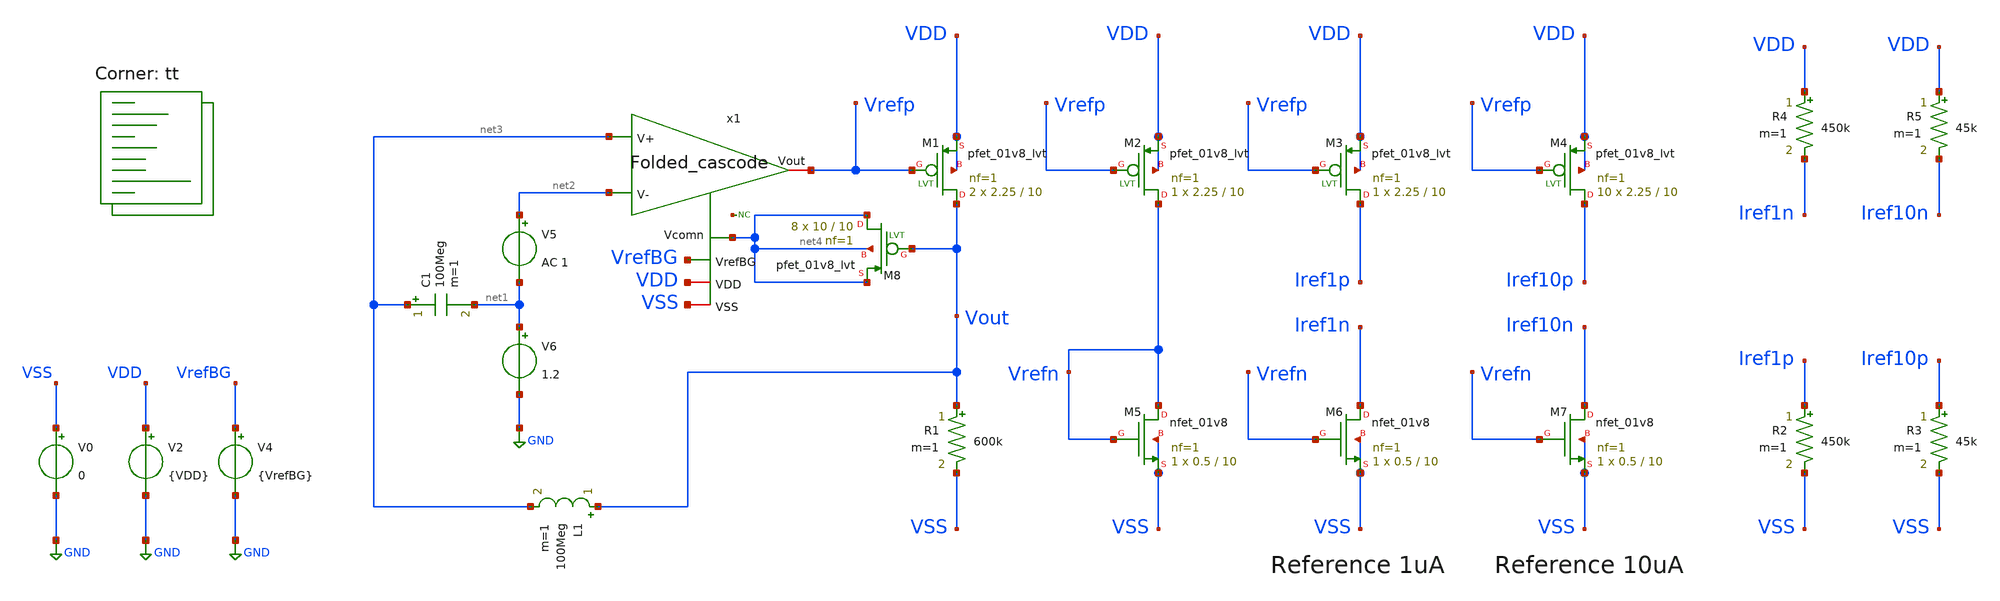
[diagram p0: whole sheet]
** sch_path: openfasoc/generators/curref-gen/sch/Current_reference_generator_AC.sch
**.subckt Current_reference_generator_AC
XM1 Vout Vrefp VDD VDD sky130_fd_pr__pfet_01v8_lvt L=10 W=2.25 nf=1 ad='int((1 + 1)/2) * 2.25 / 1 * 0.29'
+ as='int((1 + 2)/2) * 2.25 / 1 * 0.29' pd='2*int((1 + 1)/2) * (2.25 / 1 + 0.29)' ps='2*int((1 + 2)/2) * (2.25 / 1 + 0.29)'
+ nrd='0.29 / 2.25 ' nrs='0.29 / 2.25 ' sa=0 sb=0 sd=0 mult=2 m=2
R1 Vout VSS 600k m=1
XM2 Vrefn Vrefp VDD VDD sky130_fd_pr__pfet_01v8_lvt L=10 W=2.25 nf=1 ad='int((1 + 1)/2) * 2.25 / 1 * 0.29'
+ as='int((1 + 2)/2) * 2.25 / 1 * 0.29' pd='2*int((1 + 1)/2) * (2.25 / 1 + 0.29)' ps='2*int((1 + 2)/2) * (2.25 / 1 + 0.29)'
+ nrd='0.29 / 2.25 ' nrs='0.29 / 2.25 ' sa=0 sb=0 sd=0 mult=1 m=1
XM5 Vrefn Vrefn VSS VSS sky130_fd_pr__nfet_01v8 L=10 W=0.5 nf=1 ad='int((nf+1)/2) * W/nf * 0.29' as='int((nf+2)/2) * W/nf * 0.29'
+ pd='2*int((nf+1)/2) * (W/nf + 0.29)' ps='2*int((nf+2)/2) * (W/nf + 0.29)' nrd='0.29 / W' nrs='0.29 / W'
+ sa=0 sb=0 sd=0 mult=1 m=1
XM6 Iref1n Vrefn VSS VSS sky130_fd_pr__nfet_01v8 L=10 W=0.5 nf=1 ad='int((nf+1)/2) * W/nf * 0.29' as='int((nf+2)/2) * W/nf * 0.29'
+ pd='2*int((nf+1)/2) * (W/nf + 0.29)' ps='2*int((nf+2)/2) * (W/nf + 0.29)' nrd='0.29 / W' nrs='0.29 / W'
+ sa=0 sb=0 sd=0 mult=1 m=1
XM3 Iref1p Vrefp VDD VDD sky130_fd_pr__pfet_01v8_lvt L=10 W=2.25 nf=1 ad='int((1 + 1)/2) * 2.25 / 1 * 0.29'
+ as='int((1 + 2)/2) * 2.25 / 1 * 0.29' pd='2*int((1 + 1)/2) * (2.25 / 1 + 0.29)' ps='2*int((1 + 2)/2) * (2.25 / 1 + 0.29)'
+ nrd='0.29 / 2.25 ' nrs='0.29 / 2.25 ' sa=0 sb=0 sd=0 mult=1 m=1
XM7 Iref10n Vrefn VSS VSS sky130_fd_pr__nfet_01v8 L=10 W=0.5 nf=1 ad='int((nf+1)/2) * W/nf * 0.29' as='int((nf+2)/2) * W/nf * 0.29'
+ pd='2*int((nf+1)/2) * (W/nf + 0.29)' ps='2*int((nf+2)/2) * (W/nf + 0.29)' nrd='0.29 / W' nrs='0.29 / W'
+ sa=0 sb=0 sd=0 mult=1 m=1
XM4 Iref10p Vrefp VDD VDD sky130_fd_pr__pfet_01v8_lvt L=10 W=2.25 nf=1 ad='int((1 + 1)/2) * 2.25 / 1 * 0.29'
+ as='int((1 + 2)/2) * 2.25 / 1 * 0.29' pd='2*int((1 + 1)/2) * (2.25 / 1 + 0.29)' ps='2*int((1 + 2)/2) * (2.25 / 1 + 0.29)'
+ nrd='0.29 / 2.25 ' nrs='0.29 / 2.25 ' sa=0 sb=0 sd=0 mult=10 m=10
V0 VSS GND 0
V2 VDD GND {VDD}
V4 VrefBG GND {VrefBG}
R2 Iref1p VSS 450k m=1
R3 Iref10p VSS 45k m=1
R4 VDD Iref1n 450k m=1
R5 VDD Iref10n 45k m=1
L1 Vout net3 100Meg m=1
C1 net3 net1 100Meg m=1
V5 net2 net1 AC 1
V6 net1 GND 1.2
x1 Vrefp net3 net2 VrefBG VDD VSS net4 Folded_cascode
* noconn #net5
XM8 net4 Vout net4 net4 sky130_fd_pr__pfet_01v8_lvt L=10 W=10 nf=1 ad='int((1 + 1)/2) * 10 / 1 * 0.29'
+ as='int((1 + 2)/2) * 10 / 1 * 0.29' pd='2*int((1 + 1)/2) * (10 / 1 + 0.29)' ps='2*int((1 + 2)/2) * (10 / 1 + 0.29)'
+ nrd='0.29 / 10 ' nrs='0.29 / 10 ' sa=0 sb=0 sd=0 mult=8 m=8
**** begin user architecture code
.lib $::SKYWATER_MODELS/sky130.lib.spice tt



.param VDD=1.8
.param VrefBG=1.2

.save

.control

    op
    show

    write Current_reference_generator_AC.raw
    set appendwrite

    * run ac simulation
    ac dec 20 1 100e6

    * measure parameters
    let vout_mag = db(abs(v(Vout)))
    let phase = phase(v(Vout)) * 180/pi + 180

    meas ac A0 find vout_mag at=1k
    meas ac UGB when vout_mag=0 fall=1
    meas ac PM find phase when vout_mag=1

    plot (phase(v(Vout))*180/pi) db(Vout)

    write Current_reference_generator_AC.raw
.endc



**** end user architecture code
**.ends

* expanding   symbol:  /foss/designs/Folded_cascode/Folded_cascode.sym # of pins=7
** sym_path: openfasoc/generators/curref-gen/sch/Folded_cascode.sym
** sch_path: openfasoc/generators/curref-gen/sch/Folded_cascode.sch
.subckt Folded_cascode Vout V+ V- VrefBG VDD VSS Vcomn
*.ipin V+
*.ipin V-
*.ipin VrefBG
*.iopin VDD
*.iopin VSS
*.iopin Vout
*.iopin Vcomn
XM6 net2 V- net5 net5 sky130_fd_pr__nfet_01v8 L=1 W=1 nf=1 ad='int((nf+1)/2) * W/nf * 0.29' as='int((nf+2)/2) * W/nf * 0.29'
+ pd='2*int((nf+1)/2) * (W/nf + 0.29)' ps='2*int((nf+2)/2) * (W/nf + 0.29)' nrd='0.29 / W' nrs='0.29 / W'
+ sa=0 sb=0 sd=0 mult=20 m=20
XM7 Vout VB2 Vcomn VSS sky130_fd_pr__nfet_01v8 L=3 W=1 nf=1 ad='int((nf+1)/2) * W/nf * 0.29' as='int((nf+2)/2) * W/nf * 0.29'
+ pd='2*int((nf+1)/2) * (W/nf + 0.29)' ps='2*int((nf+2)/2) * (W/nf + 0.29)' nrd='0.29 / W' nrs='0.29 / W'
+ sa=0 sb=0 sd=0 mult=5 m=5
XM8 net4 VB2 net3 VSS sky130_fd_pr__nfet_01v8 L=3 W=1 nf=1 ad='int((nf+1)/2) * W/nf * 0.29' as='int((nf+2)/2) * W/nf * 0.29'
+ pd='2*int((nf+1)/2) * (W/nf + 0.29)' ps='2*int((nf+2)/2) * (W/nf + 0.29)' nrd='0.29 / W' nrs='0.29 / W'
+ sa=0 sb=0 sd=0 mult=5 m=5
XM9 Vcomn VP VSS VSS sky130_fd_pr__nfet_01v8 L=6.5 W=0.5 nf=1 ad='int((nf+1)/2) * W/nf * 0.29' as='int((nf+2)/2) * W/nf * 0.29'
+ pd='2*int((nf+1)/2) * (W/nf + 0.29)' ps='2*int((nf+2)/2) * (W/nf + 0.29)' nrd='0.29 / W' nrs='0.29 / W'
+ sa=0 sb=0 sd=0 mult=5 m=5
XM10 net3 VP VSS VSS sky130_fd_pr__nfet_01v8 L=6.5 W=0.5 nf=1 ad='int((nf+1)/2) * W/nf * 0.29' as='int((nf+2)/2) * W/nf * 0.29'
+ pd='2*int((nf+1)/2) * (W/nf + 0.29)' ps='2*int((nf+2)/2) * (W/nf + 0.29)' nrd='0.29 / W' nrs='0.29 / W'
+ sa=0 sb=0 sd=0 mult=5 m=5
XM11 net5 VP VSS VSS sky130_fd_pr__nfet_01v8 L=6.5 W=0.5 nf=1 ad='int((nf+1)/2) * W/nf * 0.29' as='int((nf+2)/2) * W/nf * 0.29'
+ pd='2*int((nf+1)/2) * (W/nf + 0.29)' ps='2*int((nf+2)/2) * (W/nf + 0.29)' nrd='0.29 / W' nrs='0.29 / W'
+ sa=0 sb=0 sd=0 mult=10 m=10
XM1 net1 V+ net5 net5 sky130_fd_pr__nfet_01v8 L=1 W=1 nf=1 ad='int((nf+1)/2) * W/nf * 0.29' as='int((nf+2)/2) * W/nf * 0.29'
+ pd='2*int((nf+1)/2) * (W/nf + 0.29)' ps='2*int((nf+2)/2) * (W/nf + 0.29)' nrd='0.29 / W' nrs='0.29 / W'
+ sa=0 sb=0 sd=0 mult=20 m=20
XM12 VP VP VSS VSS sky130_fd_pr__nfet_01v8 L=6.5 W=0.5 nf=1 ad='int((nf+1)/2) * W/nf * 0.29' as='int((nf+2)/2) * W/nf * 0.29'
+ pd='2*int((nf+1)/2) * (W/nf + 0.29)' ps='2*int((nf+2)/2) * (W/nf + 0.29)' nrd='0.29 / W' nrs='0.29 / W'
+ sa=0 sb=0 sd=0 mult=1 m=1
XM13 net6 VP VSS VSS sky130_fd_pr__nfet_01v8 L=6.5 W=0.5 nf=1 ad='int((nf+1)/2) * W/nf * 0.29' as='int((nf+2)/2) * W/nf * 0.29'
+ pd='2*int((nf+1)/2) * (W/nf + 0.29)' ps='2*int((nf+2)/2) * (W/nf + 0.29)' nrd='0.29 / W' nrs='0.29 / W'
+ sa=0 sb=0 sd=0 mult=1 m=1
XM17 VB2 VB2 VSS VSS sky130_fd_pr__nfet_01v8 L=18 W=0.42 nf=1 ad='int((nf+1)/2) * W/nf * 0.29' as='int((nf+2)/2) * W/nf * 0.29'
+ pd='2*int((nf+1)/2) * (W/nf + 0.29)' ps='2*int((nf+2)/2) * (W/nf + 0.29)' nrd='0.29 / W' nrs='0.29 / W'
+ sa=0 sb=0 sd=0 mult=1 m=1
XM18 VB2 net6 VDD VDD sky130_fd_pr__pfet_01v8_lvt L=6 W=0.5 nf=1 ad='int((1 + 1)/2) * 0.5 / 1 * 0.29'
+ as='int((1 + 2)/2) * 0.5 / 1 * 0.29' pd='2*int((1 + 1)/2) * (0.5 / 1 + 0.29)' ps='2*int((1 + 2)/2) * (0.5 / 1 + 0.29)'
+ nrd='0.29 / 0.5 ' nrs='0.29 / 0.5 ' sa=0 sb=0 sd=0 mult=4 m=4
XM15 net6 net6 VDD VDD sky130_fd_pr__pfet_01v8_lvt L=6 W=0.5 nf=1 ad='int((1 + 1)/2) * 0.5 / 1 * 0.29'
+ as='int((1 + 2)/2) * 0.5 / 1 * 0.29' pd='2*int((1 + 1)/2) * (0.5 / 1 + 0.29)' ps='2*int((1 + 2)/2) * (0.5 / 1 + 0.29)'
+ nrd='0.29 / 0.5 ' nrs='0.29 / 0.5 ' sa=0 sb=0 sd=0 mult=4 m=4
XM3 net1 net4 VDD VDD sky130_fd_pr__pfet_01v8_lvt L=3 W=1 nf=1 ad='int((1 + 1)/2) * 1 / 1 * 0.29' as='int((1 + 2)/2) * 1 / 1 * 0.29'
+ pd='2*int((1 + 1)/2) * (1 / 1 + 0.29)' ps='2*int((1 + 2)/2) * (1 / 1 + 0.29)' nrd='0.29 / 1 ' nrs='0.29 / 1 '
+ sa=0 sb=0 sd=0 mult=6 m=6
XM2 net2 net4 VDD VDD sky130_fd_pr__pfet_01v8_lvt L=3 W=1 nf=1 ad='int((1 + 1)/2) * 1 / 1 * 0.29' as='int((1 + 2)/2) * 1 / 1 * 0.29'
+ pd='2*int((1 + 1)/2) * (1 / 1 + 0.29)' ps='2*int((1 + 2)/2) * (1 / 1 + 0.29)' nrd='0.29 / 1 ' nrs='0.29 / 1 '
+ sa=0 sb=0 sd=0 mult=6 m=6
XM5 net4 VB1 net1 VDD sky130_fd_pr__pfet_01v8_lvt L=1.5 W=1 nf=1 ad='int((1 + 1)/2) * 1 / 1 * 0.29' as='int((1 + 2)/2) * 1 / 1 * 0.29'
+ pd='2*int((1 + 1)/2) * (1 / 1 + 0.29)' ps='2*int((1 + 2)/2) * (1 / 1 + 0.29)' nrd='0.29 / 1 ' nrs='0.29 / 1 '
+ sa=0 sb=0 sd=0 mult=10 m=10
XM16 Vout VB1 net2 VDD sky130_fd_pr__pfet_01v8_lvt L=1.5 W=1 nf=1 ad='int((1 + 1)/2) * 1 / 1 * 0.29'
+ as='int((1 + 2)/2) * 1 / 1 * 0.29' pd='2*int((1 + 1)/2) * (1 / 1 + 0.29)' ps='2*int((1 + 2)/2) * (1 / 1 + 0.29)'
+ nrd='0.29 / 1 ' nrs='0.29 / 1 ' sa=0 sb=0 sd=0 mult=10 m=10
XM4 VP VB1 VDD VDD sky130_fd_pr__pfet_01v8_lvt L=6 W=0.5 nf=1 ad='int((1 + 1)/2) * 0.5 / 1 * 0.29' as='int((1 + 2)/2) * 0.5 / 1 * 0.29'
+ pd='2*int((1 + 1)/2) * (0.5 / 1 + 0.29)' ps='2*int((1 + 2)/2) * (0.5 / 1 + 0.29)' nrd='0.29 / 0.5 ' nrs='0.29 / 0.5 '
+ sa=0 sb=0 sd=0 mult=1 m=1
XM14 VB1 VB1 VDD VDD sky130_fd_pr__pfet_01v8_lvt L=6 W=0.5 nf=1 ad='int((1 + 1)/2) * 0.5 / 1 * 0.29'
+ as='int((1 + 2)/2) * 0.5 / 1 * 0.29' pd='2*int((1 + 1)/2) * (0.5 / 1 + 0.29)' ps='2*int((1 + 2)/2) * (0.5 / 1 + 0.29)'
+ nrd='0.29 / 0.5 ' nrs='0.29 / 0.5 ' sa=0 sb=0 sd=0 mult=1 m=1
XM19 VB1 VrefBG VSS VSS sky130_fd_pr__nfet_01v8 L=18 W=0.45 nf=1 ad='int((nf+1)/2) * W/nf * 0.29' as='int((nf+2)/2) * W/nf * 0.29'
+ pd='2*int((nf+1)/2) * (W/nf + 0.29)' ps='2*int((nf+2)/2) * (W/nf + 0.29)' nrd='0.29 / W' nrs='0.29 / W'
+ sa=0 sb=0 sd=0 mult=1 m=1
.ends

.GLOBAL GND
.end
